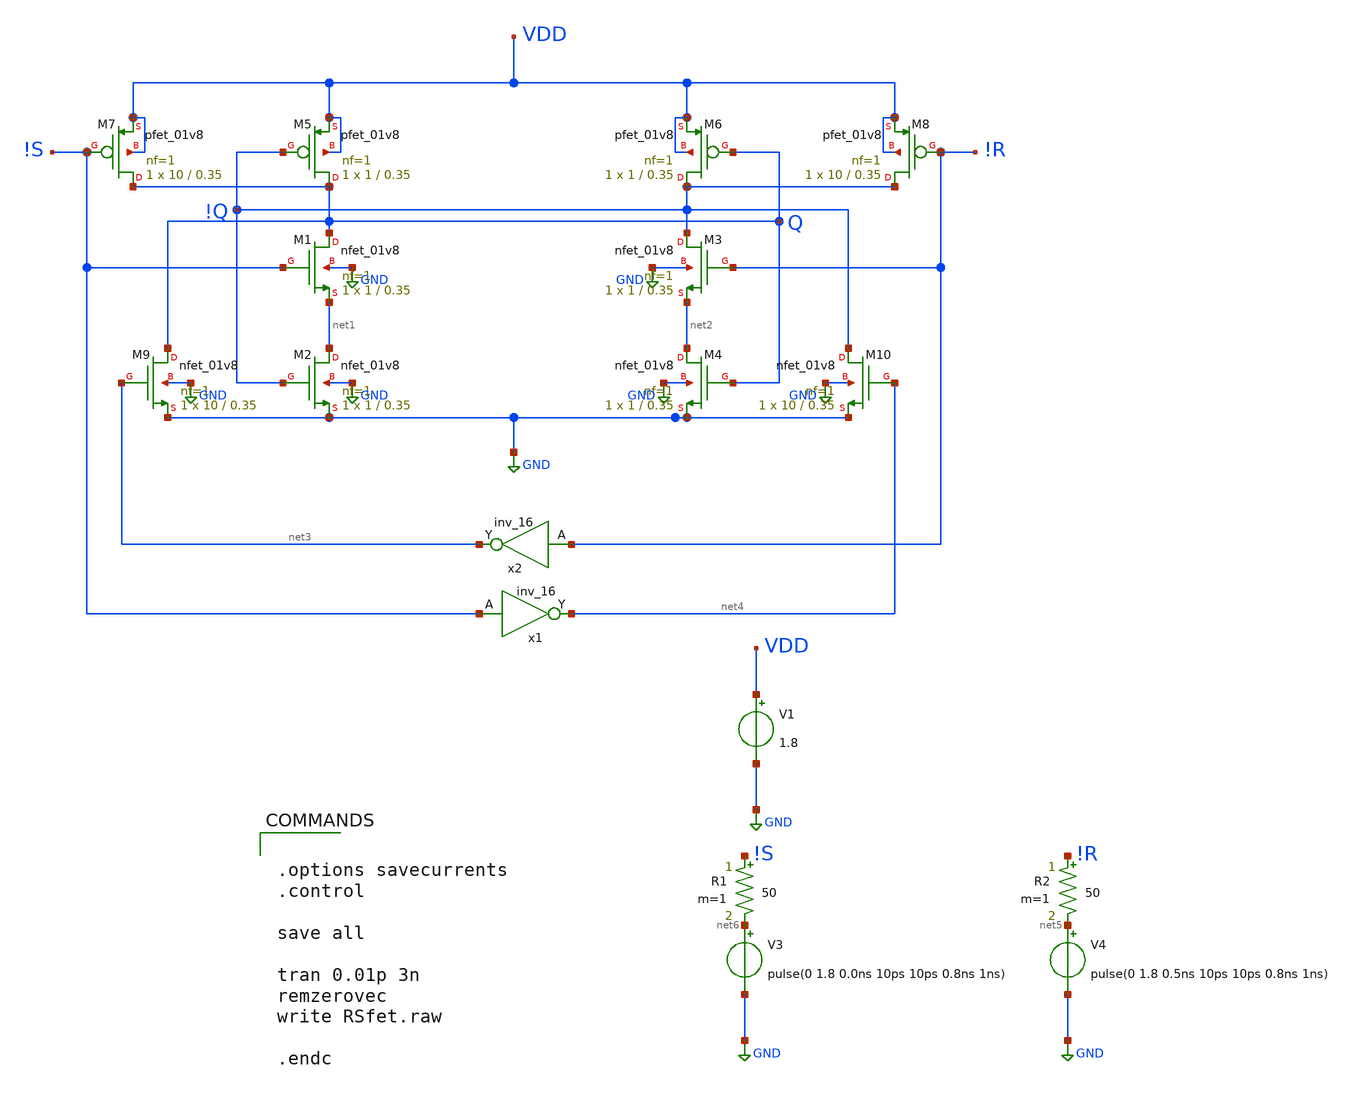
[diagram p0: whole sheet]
** sch_path: RSlatch/RSfet.sch
.lib $::SKYWATER_MODELS/sky130.lib.spice tt
.include $::SKYWATER_STDCELLS/sky130_fd_sc_hd.spice

**.subckt RSfet
V1 VDD GND 1.8
XM1 Q !S net1 GND sky130_fd_pr__nfet_01v8 L=0.35 W=1 nf=1 ad='int((nf+1)/2) * W/nf * 0.29' as='int((nf+2)/2) * W/nf * 0.29'
+ pd='2*int((nf+1)/2) * (W/nf + 0.29)' ps='2*int((nf+2)/2) * (W/nf + 0.29)' nrd='0.29 / W' nrs='0.29 / W'
+ sa=0 sb=0 sd=0 mult=1 m=1
XM2 net1 !Q GND GND sky130_fd_pr__nfet_01v8 L=0.35 W=1 nf=1 ad='int((nf+1)/2) * W/nf * 0.29' as='int((nf+2)/2) * W/nf * 0.29'
+ pd='2*int((nf+1)/2) * (W/nf + 0.29)' ps='2*int((nf+2)/2) * (W/nf + 0.29)' nrd='0.29 / W' nrs='0.29 / W'
+ sa=0 sb=0 sd=0 mult=1 m=1
XM3 !Q !R net2 GND sky130_fd_pr__nfet_01v8 L=0.35 W=1 nf=1 ad='int((nf+1)/2) * W/nf * 0.29' as='int((nf+2)/2) * W/nf * 0.29'
+ pd='2*int((nf+1)/2) * (W/nf + 0.29)' ps='2*int((nf+2)/2) * (W/nf + 0.29)' nrd='0.29 / W' nrs='0.29 / W'
+ sa=0 sb=0 sd=0 mult=1 m=1
XM4 net2 Q GND GND sky130_fd_pr__nfet_01v8 L=0.35 W=1 nf=1 ad='int((nf+1)/2) * W/nf * 0.29' as='int((nf+2)/2) * W/nf * 0.29'
+ pd='2*int((nf+1)/2) * (W/nf + 0.29)' ps='2*int((nf+2)/2) * (W/nf + 0.29)' nrd='0.29 / W' nrs='0.29 / W'
+ sa=0 sb=0 sd=0 mult=1 m=1
XM5 Q !Q VDD VDD sky130_fd_pr__pfet_01v8 L=0.35 W=1 nf=1 ad='int((nf+1)/2) * W/nf * 0.29' as='int((nf+2)/2) * W/nf * 0.29'
+ pd='2*int((nf+1)/2) * (W/nf + 0.29)' ps='2*int((nf+2)/2) * (W/nf + 0.29)' nrd='0.29 / W' nrs='0.29 / W'
+ sa=0 sb=0 sd=0 mult=1 m=1
XM6 !Q Q VDD VDD sky130_fd_pr__pfet_01v8 L=0.35 W=1 nf=1 ad='int((nf+1)/2) * W/nf * 0.29' as='int((nf+2)/2) * W/nf * 0.29'
+ pd='2*int((nf+1)/2) * (W/nf + 0.29)' ps='2*int((nf+2)/2) * (W/nf + 0.29)' nrd='0.29 / W' nrs='0.29 / W'
+ sa=0 sb=0 sd=0 mult=1 m=1
XM7 Q !S VDD VDD sky130_fd_pr__pfet_01v8 L=0.35 W=10 nf=1 ad='int((nf+1)/2) * W/nf * 0.29' as='int((nf+2)/2) * W/nf * 0.29'
+ pd='2*int((nf+1)/2) * (W/nf + 0.29)' ps='2*int((nf+2)/2) * (W/nf + 0.29)' nrd='0.29 / W' nrs='0.29 / W'
+ sa=0 sb=0 sd=0 mult=1 m=1
XM8 !Q !R VDD VDD sky130_fd_pr__pfet_01v8 L=0.35 W=10 nf=1 ad='int((nf+1)/2) * W/nf * 0.29' as='int((nf+2)/2) * W/nf * 0.29'
+ pd='2*int((nf+1)/2) * (W/nf + 0.29)' ps='2*int((nf+2)/2) * (W/nf + 0.29)' nrd='0.29 / W' nrs='0.29 / W'
+ sa=0 sb=0 sd=0 mult=1 m=1
V4 net5 GND pulse(0 1.8 0.5ns 10ps 10ps 0.8ns 1ns)
V3 net6 GND pulse(0 1.8 0.0ns 10ps 10ps 0.8ns 1ns)
XM9 Q net3 GND GND sky130_fd_pr__nfet_01v8 L=0.35 W=10 nf=1 ad='int((nf+1)/2) * W/nf * 0.29' as='int((nf+2)/2) * W/nf * 0.29'
+ pd='2*int((nf+1)/2) * (W/nf + 0.29)' ps='2*int((nf+2)/2) * (W/nf + 0.29)' nrd='0.29 / W' nrs='0.29 / W'
+ sa=0 sb=0 sd=0 mult=1 m=1
XM10 !Q net4 GND GND sky130_fd_pr__nfet_01v8 L=0.35 W=10 nf=1 ad='int((nf+1)/2) * W/nf * 0.29' as='int((nf+2)/2) * W/nf * 0.29'
+ pd='2*int((nf+1)/2) * (W/nf + 0.29)' ps='2*int((nf+2)/2) * (W/nf + 0.29)' nrd='0.29 / W' nrs='0.29 / W'
+ sa=0 sb=0 sd=0 mult=1 m=1
x2 !R GND GND VDD VDD net3 sky130_fd_sc_hd__inv_16
x1 !S GND GND VDD VDD net4 sky130_fd_sc_hd__inv_16
R1 !S net6 50 m=1
R2 !R net5 50 m=1
**** begin user architecture code


.options savecurrents
.control

save all

tran 0.01p 3n
remzerovec
write RSfet.raw

.endc


**** end user architecture code
**.ends
.GLOBAL GND
.end
